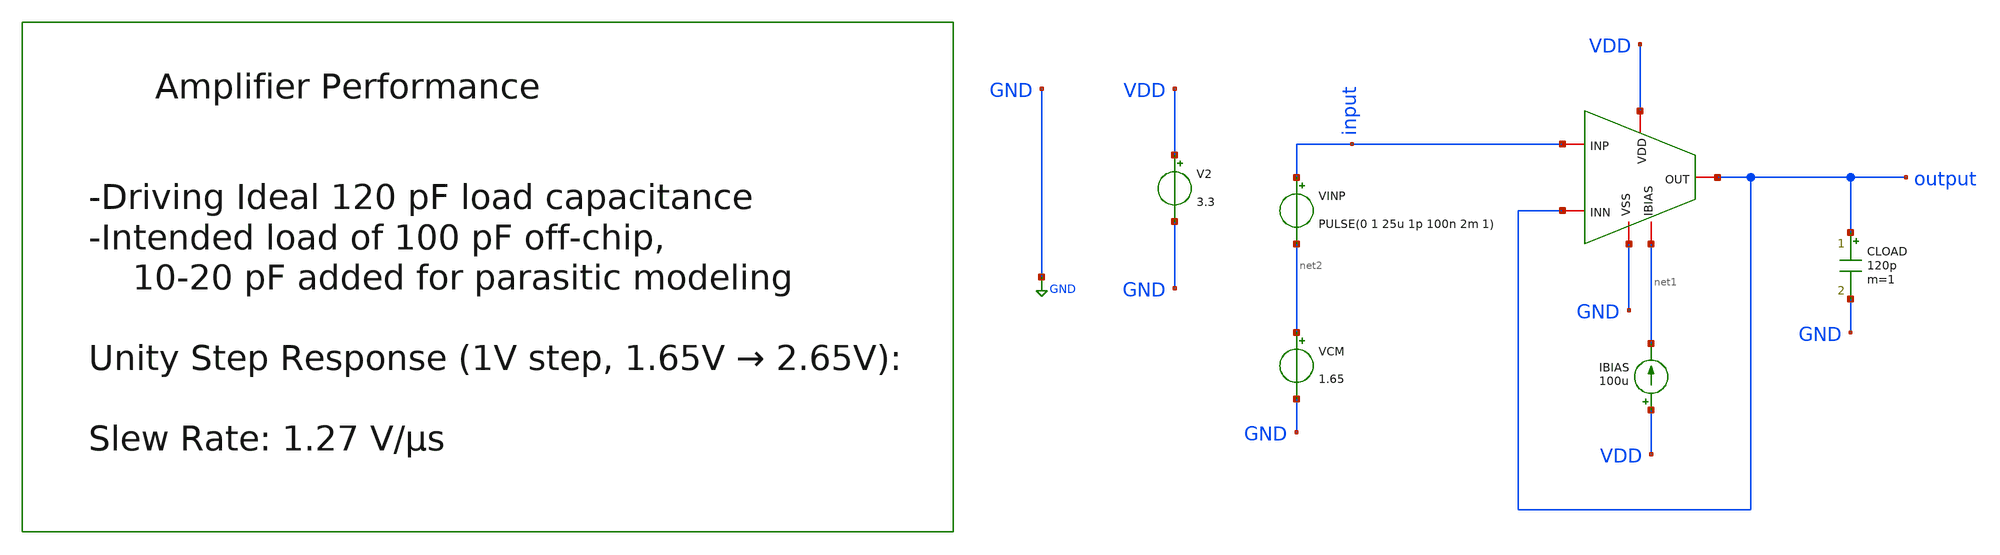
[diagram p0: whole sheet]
** sch_path: designs/libs/core_amps/ota_folded_cascode/tb/unity_step_tran_SR_tb.sch
**.subckt unity_step_tran_SR_tb
IBIAS VDD net1 100u
V2 VDD GND 3.3
CLOAD output GND 120p m=1
VINP input net2 PULSE(0 1 25u 1p 100n 2m 1)
VCM net2 GND 1.65
x1 VDD GND output input output net1 ota_folded_cascode
**** begin user architecture code

.include $::180MCU_MODELS/design.ngspice
.lib $::180MCU_MODELS/sm141064.ngspice typical



.control
tran 1n 100u
meas tran v_before find v(output) at=24u
meas tran v_after find v(output) at=90u
let v_20 = v_before + 0.2 * (v_after - v_before)
let v_80 = v_before + 0.8 * (v_after - v_before)
meas tran t_20 when v(output) = v_20 rise = 1 from = 25u
meas tran t_80 when v(output) = v_80 rise = 1 from = 25u
let slew_rate = (v_80 - v_20) / (t_80 - t_20)
print v_before v_after
print slew_rate

plot v(input) v(output)
.endc



**** end user architecture code
**.ends
.GLOBAL GND
.end
